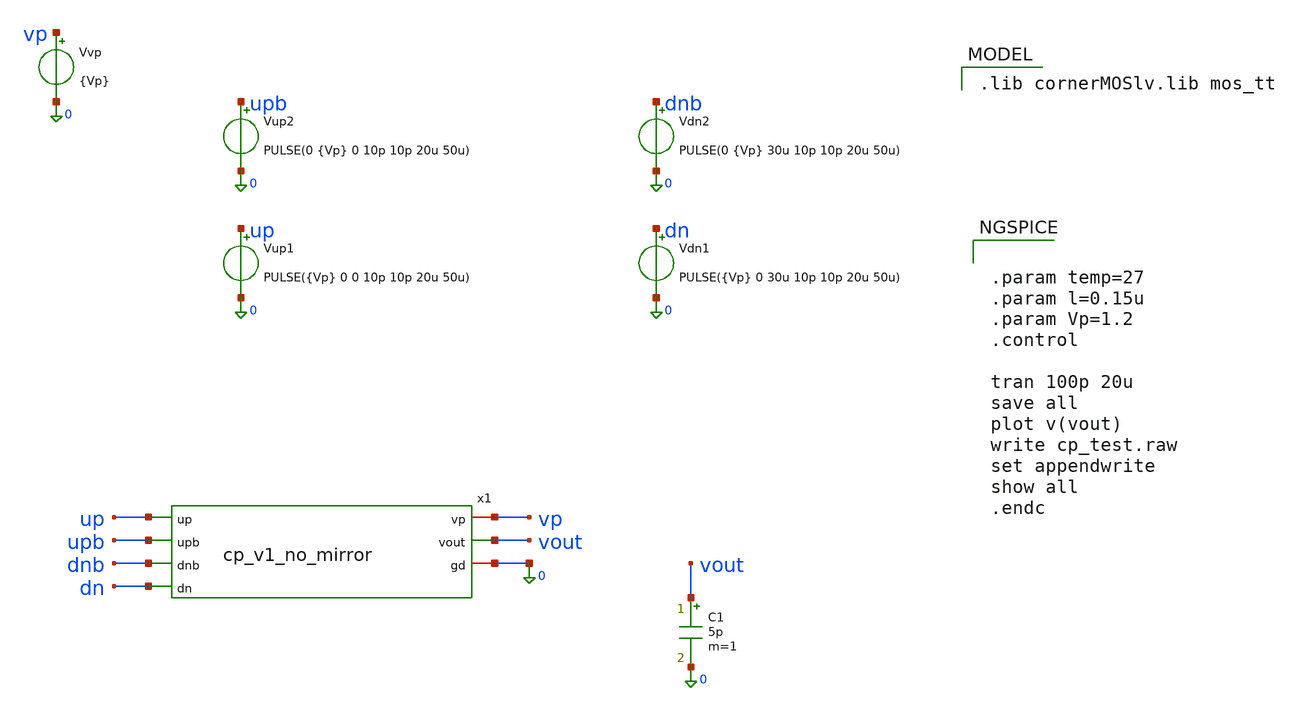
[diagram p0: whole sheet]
** sch_path: charge_pump/cp_v1_tb_tran.sch
**.subckt cp_v1_tb_tran
Vvp vp 0 {Vp}
Vup1 up 0 PULSE({Vp} 0 0 10p 10p 20u 50u)
Vdn1 dn 0 PULSE({Vp} 0 30u 10p 10p 20u 50u)
C1 vout 0 5p m=1
Vup2 upb 0 PULSE(0 {Vp} 0 10p 10p 20u 50u)
Vdn2 dnb 0 PULSE(0 {Vp} 30u 10p 10p 20u 50u)
x1 vp up upb vout dnb dn 0 cp_v1_no_mirror
**** begin user architecture code
 .lib cornerMOSlv.lib mos_tt



.param temp=27
.param l=0.15u
.param Vp=1.2
.control

tran 100p 20u
save all
plot v(vout)
write cp_test.raw
set appendwrite
show all
.endc


**** end user architecture code
**.ends
.end
